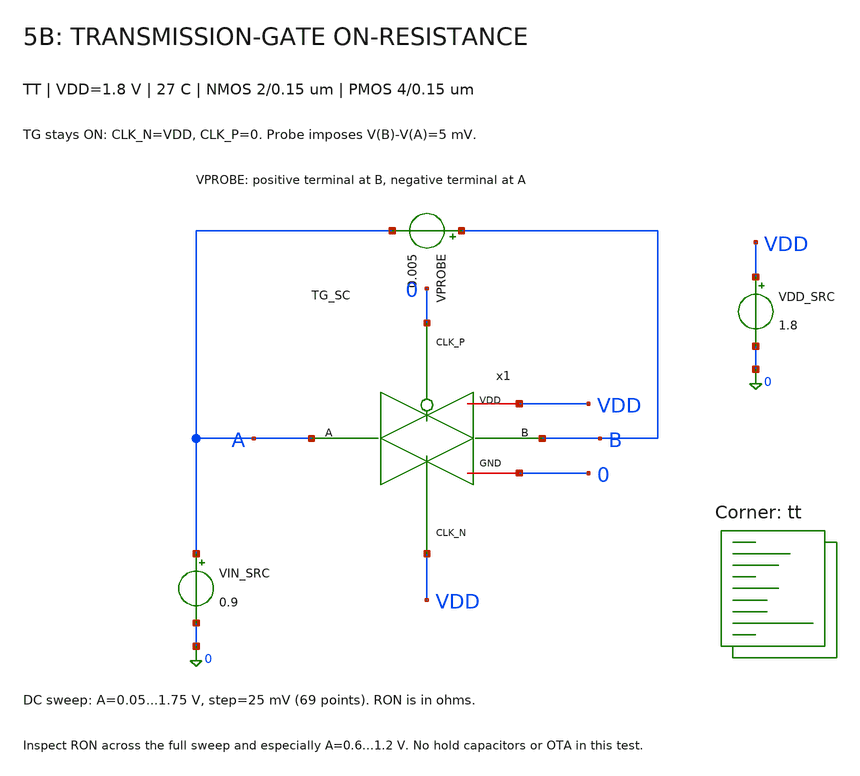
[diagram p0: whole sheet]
** sch_path: blocks/05_Switch_Network/sim/tb_5B_ron.sch
**.subckt tb_5B_ron
VPROBE B A 0.005
.save i(vprobe)
VIN_SRC A 0 0.9
VDD_SRC VDD 0 1.8
x1 A B 0 VDD VDD 0 TG_SC
**** begin user architecture code
.lib $::SKYWATER_MODELS/sky130.lib.spice tt


* Requires TG_SC.sym and TG_SC.sch in the same directory.
* Expected DUT pin order: A B CLK_P CLK_N VDD GND.
* Expected exported sources: VPROBE B A 0.005; VIN_SRC A 0 0.9.
.option scale=1e-6 reltol=1e-5 abstol=1e-15 vntol=1e-8
.temp 27
.control
save all
set wr_singlescale
set wr_vecnames
set numdgt=15
dc VIN_SRC 0.05 1.75 0.025
let RON = abs((v(B)-v(A))/i(VPROBE))
meas dc RON_MIN MIN RON
meas dc RON_MAX MAX RON
meas dc RON_060 FIND RON AT=0.6
meas dc RON_090 FIND RON AT=0.9
meas dc RON_120 FIND RON AT=1.2
wrdata tb_5B_ron.dat v(A) v(B) i(VPROBE) RON
plot RON
.endc


**** end user architecture code
**.ends

* expanding   symbol:  blocks/05_Switch_Network/xschem/TG_SC.sym # of pins=6
** sym_path: blocks/05_Switch_Network/xschem/TG_SC.sym
** sch_path: blocks/05_Switch_Network/xschem/TG_SC.sch
.subckt TG_SC A B CLK_P CLK_N VDD GND
*.iopin A
*.iopin B
*.ipin CLK_P
*.ipin CLK_N
*.iopin VDD
*.iopin GND
XMP A CLK_P B VDD sky130_fd_pr__pfet_01v8 L=0.15 W=4 nf=1 ad='int((1 + 1)/2) * 4 / 1 * 0.29' as='int((1 + 2)/2) * 4 / 1 * 0.29'
+ pd='2*int((1 + 1)/2) * (4 / 1 + 0.29)' ps='2*int((1 + 2)/2) * (4 / 1 + 0.29)' nrd='0.29 / 4 ' nrs='0.29 / 4 '
+ sa=0 sb=0 sd=0 mult=1 m=1
XMN A CLK_N B GND sky130_fd_pr__nfet_01v8 L=0.15 W=2 nf=1 ad='int((1 + 1)/2) * 2 / 1 * 0.29' as='int((1 + 2)/2) * 2 / 1 * 0.29'
+ pd='2*int((1 + 1)/2) * (2 / 1 + 0.29)' ps='2*int((1 + 2)/2) * (2 / 1 + 0.29)' nrd='0.29 / 2 ' nrs='0.29 / 2 '
+ sa=0 sb=0 sd=0 mult=1 m=1
.ends

.end
